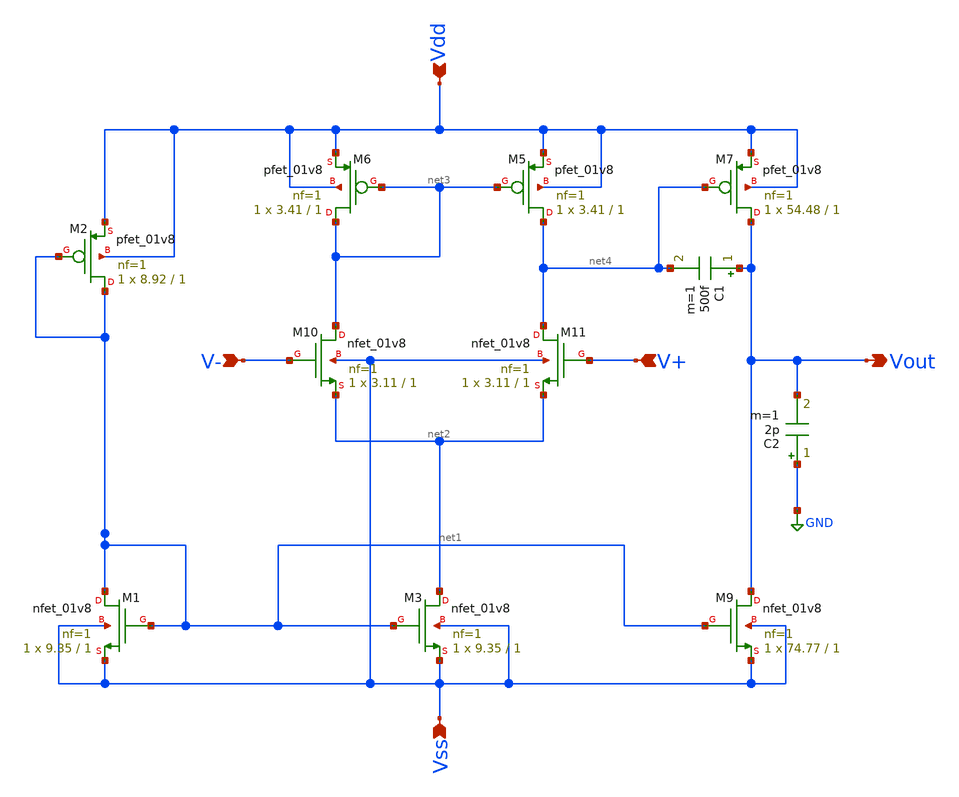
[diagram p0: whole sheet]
** sch_path: xschem/op_amp_2.sch
**.subckt op_amp_2 Vout Vdd Vss V+ V-
*.opin Vout
*.ipin Vdd
*.ipin Vss
*.ipin V+
*.ipin V-
XM1 net1 net1 Vss Vss sky130_fd_pr__nfet_01v8 L=1 W=9.35 nf=1 ad='int((1 + 1)/2) * 9.35 / 1 * 0.29' as='int((1 + 2)/2) * 9.35 / 1 * 0.29'
+ pd='2*int((1 + 1)/2) * (9.35 / 1 + 0.29)' ps='2*int((1 + 2)/2) * (9.35 / 1 + 0.29)' nrd='0.29 / 9.35 '
+ nrs='0.29 / 9.35 ' sa=0 sb=0 sd=0 mult=1 m=1
XM3 net2 net1 Vss Vss sky130_fd_pr__nfet_01v8 L=1 W=9.35 nf=1 ad='int((1 + 1)/2) * 9.35 / 1 * 0.29' as='int((1 + 2)/2) * 9.35 / 1 * 0.29'
+ pd='2*int((1 + 1)/2) * (9.35 / 1 + 0.29)' ps='2*int((1 + 2)/2) * (9.35 / 1 + 0.29)' nrd='0.29 / 9.35 '
+ nrs='0.29 / 9.35 ' sa=0 sb=0 sd=0 mult=1 m=1
XM10 net3 V- net2 Vss sky130_fd_pr__nfet_01v8 L=1 W=3.11 nf=1 ad='int((1 + 1)/2) * 3.11 / 1 * 0.29' as='int((1 + 2)/2) * 3.11 / 1 * 0.29'
+ pd='2*int((1 + 1)/2) * (3.11 / 1 + 0.29)' ps='2*int((1 + 2)/2) * (3.11 / 1 + 0.29)' nrd='0.29 / 3.11 '
+ nrs='0.29 / 3.11 ' sa=0 sb=0 sd=0 mult=1 m=1
XM11 net4 V+ net2 Vss sky130_fd_pr__nfet_01v8 L=1 W=3.11 nf=1 ad='int((1 + 1)/2) * 3.11 / 1 * 0.29' as='int((1 + 2)/2) * 3.11 / 1 * 0.29'
+ pd='2*int((1 + 1)/2) * (3.11 / 1 + 0.29)' ps='2*int((1 + 2)/2) * (3.11 / 1 + 0.29)' nrd='0.29 / 3.11 '
+ nrs='0.29 / 3.11 ' sa=0 sb=0 sd=0 mult=1 m=1
XM5 net4 net3 Vdd Vdd sky130_fd_pr__pfet_01v8 L=1 W=3.41 nf=1 ad='int((1 + 1)/2) * 3.41 / 1 * 0.29' as='int((1 + 2)/2) * 3.41 / 1 * 0.29'
+ pd='2*int((1 + 1)/2) * (3.41 / 1 + 0.29)' ps='2*int((1 + 2)/2) * (3.41 / 1 + 0.29)' nrd='0.29 / 3.41 '
+ nrs='0.29 / 3.41 ' sa=0 sb=0 sd=0 mult=1 m=1
XM6 net3 net3 Vdd Vdd sky130_fd_pr__pfet_01v8 L=1 W=3.41 nf=1 ad='int((1 + 1)/2) * 3.41 / 1 * 0.29' as='int((1 + 2)/2) * 3.41 / 1 * 0.29'
+ pd='2*int((1 + 1)/2) * (3.41 / 1 + 0.29)' ps='2*int((1 + 2)/2) * (3.41 / 1 + 0.29)' nrd='0.29 / 3.41 '
+ nrs='0.29 / 3.41 ' sa=0 sb=0 sd=0 mult=1 m=1
C1 Vout net4 500f m=1
C2 GND Vout 2p m=1
XM2 net1 net1 Vdd Vdd sky130_fd_pr__pfet_01v8 L=1 W=8.92 nf=1 ad='int((1 + 1)/2) * 8.92 / 1 * 0.29' as='int((1 + 2)/2) * 8.92 / 1 * 0.29'
+ pd='2*int((1 + 1)/2) * (8.92 / 1 + 0.29)' ps='2*int((1 + 2)/2) * (8.92 / 1 + 0.29)' nrd='0.29 / 8.92 '
+ nrs='0.29 / 8.92 ' sa=0 sb=0 sd=0 mult=1 m=1
XM7 Vout net4 Vdd Vdd sky130_fd_pr__pfet_01v8 L=1 W=54.48 nf=1 ad='int((1 + 1)/2) * 54.48 / 1 * 0.29'
+ as='int((1 + 2)/2) * 54.48 / 1 * 0.29' pd='2*int((1 + 1)/2) * (54.48 / 1 + 0.29)' ps='2*int((1 + 2)/2) * (54.48 / 1 + 0.29)'
+ nrd='0.29 / 54.48 ' nrs='0.29 / 54.48 ' sa=0 sb=0 sd=0 mult=1 m=1
XM9 Vout net1 Vss Vss sky130_fd_pr__nfet_01v8 L=1 W=74.77 nf=1 ad='int((1 + 1)/2) * 74.77 / 1 * 0.29'
+ as='int((1 + 2)/2) * 74.77 / 1 * 0.29' pd='2*int((1 + 1)/2) * (74.77 / 1 + 0.29)' ps='2*int((1 + 2)/2) * (74.77 / 1 + 0.29)'
+ nrd='0.29 / 74.77 ' nrs='0.29 / 74.77 ' sa=0 sb=0 sd=0 mult=1 m=1
**.ends
.GLOBAL GND
.end
